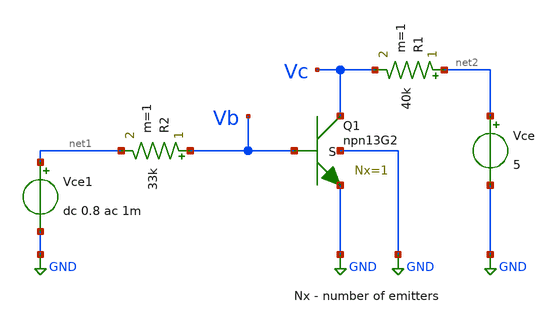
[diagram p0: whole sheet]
** sch_path: ihp-sg13g2/xschem_libs/sg13g2_tests_ase/mc_hbt_13g2_ac/schematic/mc_hbt_13g2_ac.sch
* Copyright 2023 IHP PDK Authors
**.subckt mc_hbt_13g2_ac
Vce net2 GND 5
R1 net2 Vc 40k m=1
Vce1 net1 GND dc 0.8 ac 1m
R2 Vb net1 33k m=1
XQ1 Vc Vb GND GND npn13G2 Nx=1 mm_ok=1
**.ends
.GLOBAL GND
.end
